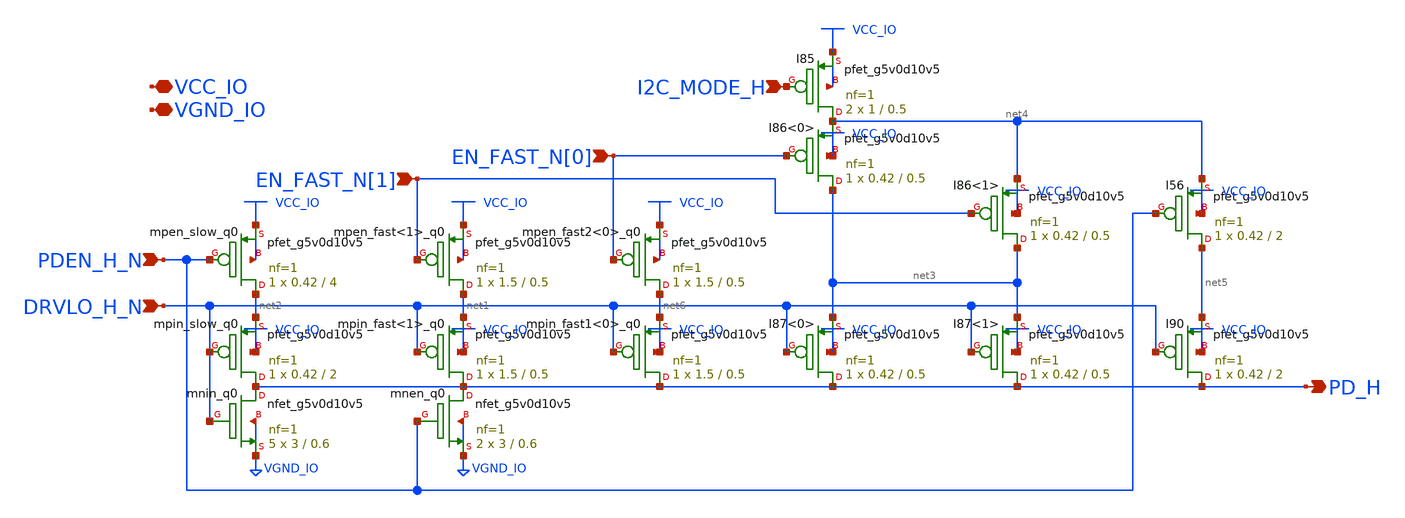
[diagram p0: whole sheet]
** sch_path: gpiov2_pdpredrvr_strong_nr3.sch
* Copyright 2023 David Mitchell Bailey
* Licensed under the Apache License, Version 2.0 (the "License");
* you may not use this file except in compliance with the License.
* You may obtain a copy of the License at
* https://www.apache.org/licenses/LICENSE-2.0
* Unless required by applicable law or agreed to in writing, software
* distributed under the License is distributed on an "AS IS" BASIS,
* WITHOUT WARRANTIES OR CONDITIONS OF ANY KIND, either express or implied.
* See the License for the specific language governing permissions and
* limitations under the License.
**.subckt gpiov2_pdpredrvr_strong_nr3 PDEN_H_N VCC_IO VGND_IO DRVLO_H_N I2C_MODE_H EN_FAST_N[1]
*+ EN_FAST_N[0] PD_H
*.ipin PDEN_H_N
*.iopin VCC_IO
*.iopin VGND_IO
*.ipin DRVLO_H_N
*.ipin I2C_MODE_H
*.ipin EN_FAST_N[1]
*.ipin EN_FAST_N[0]
*.opin PD_H
Xmpin_slow_q0 PD_H DRVLO_H_N net2 VCC_IO sky130_fd_pr__pfet_g5v0d10v5 L=2 W=0.42 nf=1 ad='int((nf+1)/2) * W/nf * 0.29'
+ as='int((nf+2)/2) * W/nf * 0.29' pd='2*int((nf+1)/2) * (W/nf + 0.29)' ps='2*int((nf+2)/2) * (W/nf + 0.29)'
+ nrd='0.29 / W' nrs='0.29 / W' sa=0 sb=0 sd=0 mult=1 m=1
Xmpen_slow_q0 net2 PDEN_H_N VCC_IO VCC_IO sky130_fd_pr__pfet_g5v0d10v5 L=4 W=0.42 nf=1 ad='int((nf+1)/2) * W/nf * 0.29'
+ as='int((nf+2)/2) * W/nf * 0.29' pd='2*int((nf+1)/2) * (W/nf + 0.29)' ps='2*int((nf+2)/2) * (W/nf + 0.29)'
+ nrd='0.29 / W' nrs='0.29 / W' sa=0 sb=0 sd=0 mult=1 m=1
Xmpin_fast<1>_q0 PD_H DRVLO_H_N net1 VCC_IO sky130_fd_pr__pfet_g5v0d10v5 L=0.5 W=1.5 nf=1 ad='int((nf+1)/2) * W/nf * 0.29'
+ as='int((nf+2)/2) * W/nf * 0.29' pd='2*int((nf+1)/2) * (W/nf + 0.29)' ps='2*int((nf+2)/2) * (W/nf + 0.29)'
+ nrd='0.29 / W' nrs='0.29 / W' sa=0 sb=0 sd=0 mult=1 m=1
Xmpen_fast<1>_q0 net1 EN_FAST_N[1] VCC_IO VCC_IO sky130_fd_pr__pfet_g5v0d10v5 L=0.5 W=1.5 nf=1 ad='int((nf+1)/2) * W/nf * 0.29'
+ as='int((nf+2)/2) * W/nf * 0.29' pd='2*int((nf+1)/2) * (W/nf + 0.29)' ps='2*int((nf+2)/2) * (W/nf + 0.29)'
+ nrd='0.29 / W' nrs='0.29 / W' sa=0 sb=0 sd=0 mult=1 m=1
Xmnin_q0 PD_H DRVLO_H_N VGND_IO VGND_IO sky130_fd_pr__nfet_g5v0d10v5 L=0.6 W=3 nf=1 ad='int((nf+1)/2) * W/nf * 0.29'
+ as='int((nf+2)/2) * W/nf * 0.29' pd='2*int((nf+1)/2) * (W/nf + 0.29)' ps='2*int((nf+2)/2) * (W/nf + 0.29)'
+ nrd='0.29 / W' nrs='0.29 / W' sa=0 sb=0 sd=0 mult=5 m=5
Xmnen_q0 PD_H PDEN_H_N VGND_IO VGND_IO sky130_fd_pr__nfet_g5v0d10v5 L=0.6 W=3 nf=1 ad='int((nf+1)/2) * W/nf * 0.29'
+ as='int((nf+2)/2) * W/nf * 0.29' pd='2*int((nf+1)/2) * (W/nf + 0.29)' ps='2*int((nf+2)/2) * (W/nf + 0.29)'
+ nrd='0.29 / W' nrs='0.29 / W' sa=0 sb=0 sd=0 mult=2 m=2
XI87<0> PD_H DRVLO_H_N net3 VCC_IO sky130_fd_pr__pfet_g5v0d10v5 L=0.5 W=0.42 nf=1 ad='int((nf+1)/2) * W/nf * 0.29'
+ as='int((nf+2)/2) * W/nf * 0.29' pd='2*int((nf+1)/2) * (W/nf + 0.29)' ps='2*int((nf+2)/2) * (W/nf + 0.29)'
+ nrd='0.29 / W' nrs='0.29 / W' sa=0 sb=0 sd=0 mult=1 m=1
XI85 net4 I2C_MODE_H VCC_IO VCC_IO sky130_fd_pr__pfet_g5v0d10v5 L=0.5 W=1 nf=1 ad='int((nf+1)/2) * W/nf * 0.29'
+ as='int((nf+2)/2) * W/nf * 0.29' pd='2*int((nf+1)/2) * (W/nf + 0.29)' ps='2*int((nf+2)/2) * (W/nf + 0.29)'
+ nrd='0.29 / W' nrs='0.29 / W' sa=0 sb=0 sd=0 mult=2 m=2
XI90 PD_H DRVLO_H_N net5 VCC_IO sky130_fd_pr__pfet_g5v0d10v5 L=2 W=0.42 nf=1 ad='int((nf+1)/2) * W/nf * 0.29'
+ as='int((nf+2)/2) * W/nf * 0.29' pd='2*int((nf+1)/2) * (W/nf + 0.29)' ps='2*int((nf+2)/2) * (W/nf + 0.29)'
+ nrd='0.29 / W' nrs='0.29 / W' sa=0 sb=0 sd=0 mult=1 m=1
XI86<0> net3 EN_FAST_N[0] net4 VCC_IO sky130_fd_pr__pfet_g5v0d10v5 L=0.5 W=0.42 nf=1 ad='int((nf+1)/2) * W/nf * 0.29'
+ as='int((nf+2)/2) * W/nf * 0.29' pd='2*int((nf+1)/2) * (W/nf + 0.29)' ps='2*int((nf+2)/2) * (W/nf + 0.29)'
+ nrd='0.29 / W' nrs='0.29 / W' sa=0 sb=0 sd=0 mult=1 m=1
XI56 net5 PDEN_H_N net4 VCC_IO sky130_fd_pr__pfet_g5v0d10v5 L=2 W=0.42 nf=1 ad='int((nf+1)/2) * W/nf * 0.29'
+ as='int((nf+2)/2) * W/nf * 0.29' pd='2*int((nf+1)/2) * (W/nf + 0.29)' ps='2*int((nf+2)/2) * (W/nf + 0.29)'
+ nrd='0.29 / W' nrs='0.29 / W' sa=0 sb=0 sd=0 mult=1 m=1
XI87<1> PD_H DRVLO_H_N net3 VCC_IO sky130_fd_pr__pfet_g5v0d10v5 L=0.5 W=0.42 nf=1 ad='int((nf+1)/2) * W/nf * 0.29'
+ as='int((nf+2)/2) * W/nf * 0.29' pd='2*int((nf+1)/2) * (W/nf + 0.29)' ps='2*int((nf+2)/2) * (W/nf + 0.29)'
+ nrd='0.29 / W' nrs='0.29 / W' sa=0 sb=0 sd=0 mult=1 m=1
XI86<1> net3 EN_FAST_N[1] net4 VCC_IO sky130_fd_pr__pfet_g5v0d10v5 L=0.5 W=0.42 nf=1 ad='int((nf+1)/2) * W/nf * 0.29'
+ as='int((nf+2)/2) * W/nf * 0.29' pd='2*int((nf+1)/2) * (W/nf + 0.29)' ps='2*int((nf+2)/2) * (W/nf + 0.29)'
+ nrd='0.29 / W' nrs='0.29 / W' sa=0 sb=0 sd=0 mult=1 m=1
Xmpin_fast1<0>_q0 PD_H DRVLO_H_N net6 VCC_IO sky130_fd_pr__pfet_g5v0d10v5 L=0.5 W=1.5 nf=1 ad='int((nf+1)/2) * W/nf * 0.29'
+ as='int((nf+2)/2) * W/nf * 0.29' pd='2*int((nf+1)/2) * (W/nf + 0.29)' ps='2*int((nf+2)/2) * (W/nf + 0.29)'
+ nrd='0.29 / W' nrs='0.29 / W' sa=0 sb=0 sd=0 mult=1 m=1
Xmpen_fast2<0>_q0 net6 EN_FAST_N[0] VCC_IO VCC_IO sky130_fd_pr__pfet_g5v0d10v5 L=0.5 W=1.5 nf=1 ad='int((nf+1)/2) * W/nf * 0.29'
+ as='int((nf+2)/2) * W/nf * 0.29' pd='2*int((nf+1)/2) * (W/nf + 0.29)' ps='2*int((nf+2)/2) * (W/nf + 0.29)'
+ nrd='0.29 / W' nrs='0.29 / W' sa=0 sb=0 sd=0 mult=1 m=1
**.ends
.end
